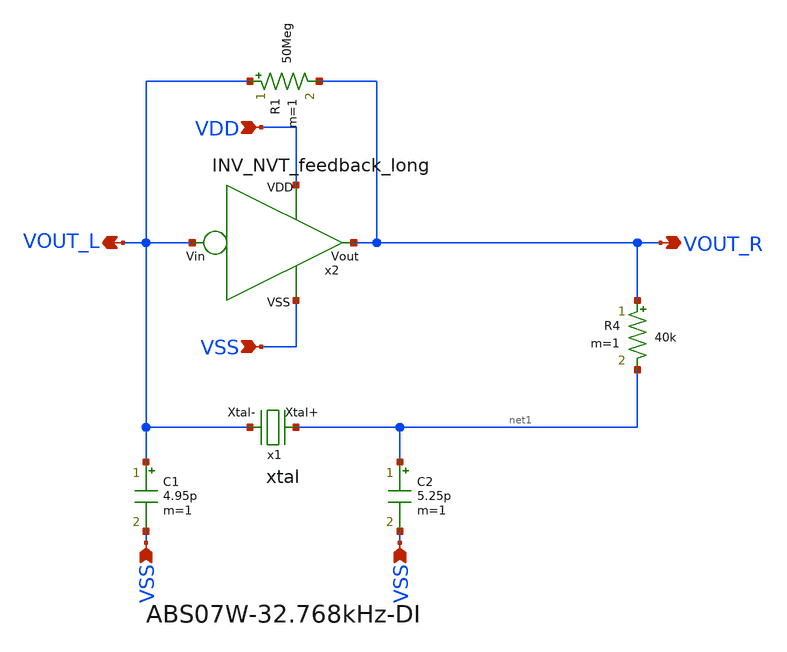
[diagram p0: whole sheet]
** sch_path: design/THESIS_EXP_RO_INVERTER_SKY130A/xtal_osc_NVT_L.sch
**.subckt xtal_osc_NVT_L VSS VSS VOUT_R VOUT_L VDD VSS
*.ipin VSS
*.ipin VSS
*.opin VOUT_R
*.opin VOUT_L
*.ipin VDD
*.ipin VSS
x1 net1 VOUT_L xtal
C1 VOUT_L VSS 4.95p m=1
C2 net1 VSS 5.25p m=1
R1 VOUT_L VOUT_R 50Meg m=1
R4 VOUT_R net1 40k m=1
x2 VDD VSS VOUT_R VOUT_L INV_NVT_feedback_long
**.ends

* expanding   symbol:  THESIS_EXP_RO_INVERTER_SKY130A/xtal.sym # of pins=2
** sym_path: design/THESIS_EXP_RO_INVERTER_SKY130A/xtal.sym
** sch_path: design/THESIS_EXP_RO_INVERTER_SKY130A/xtal.sch
.subckt xtal Xtal+ Xtal-
*.iopin Xtal+
*.iopin Xtal-
R1 Xtal+ net1 38.194k m=1
C1 net1 net2 4.68f m=1
L1 net2 Xtal- 5048.571 m=1
C2 Xtal+ Xtal- 1.15p m=1
.ends


* expanding   symbol:  THESIS_EXP_RO_INVERTER_SKY130A/INV_NVT_feedback_long.sym # of pins=4
** sym_path: design/THESIS_EXP_RO_INVERTER_SKY130A/INV_NVT_feedback_long.sym
** sch_path: design/THESIS_EXP_RO_INVERTER_SKY130A/INV_NVT_feedback_long.sch
.subckt INV_NVT_feedback_long VDD VSS Vout Vin
*.ipin VSS
*.ipin Vin
*.opin Vout
*.ipin VDD
XM1 Vout Vin VDD VDD sky130_fd_pr__pfet_01v8_lvt L=0.35 W=7 nf=1 ad='int((nf+1)/2) * W/nf * 0.29' as='int((nf+2)/2) * W/nf * 0.29'
+ pd='2*int((nf+1)/2) * (W/nf + 0.29)' ps='2*int((nf+2)/2) * (W/nf + 0.29)' nrd='0.29 / W' nrs='0.29 / W'
+ sa=0 sb=0 sd=0 mult=m_alpha m=m_alpha
XM2 Vout Vin vn VSS sky130_fd_pr__nfet_03v3_nvt L=0.8 W=0.42 nf=1 ad='int((nf+1)/2) * W/nf * 0.29' as='int((nf+2)/2) * W/nf * 0.29'
+ pd='2*int((nf+1)/2) * (W/nf + 0.29)' ps='2*int((nf+2)/2) * (W/nf + 0.29)' nrd='0.29 / W' nrs='0.29 / W'
+ sa=0 sb=0 sd=0 mult=m_beta m=m_beta
XM3 vn Vin VSS VSS sky130_fd_pr__nfet_03v3_nvt L=0.8 W=0.42 nf=1 ad='int((nf+1)/2) * W/nf * 0.29' as='int((nf+2)/2) * W/nf * 0.29'
+ pd='2*int((nf+1)/2) * (W/nf + 0.29)' ps='2*int((nf+2)/2) * (W/nf + 0.29)' nrd='0.29 / W' nrs='0.29 / W'
+ sa=0 sb=0 sd=0 mult=m_I0 m=m_I0
XM4 VDD Vout vn VSS sky130_fd_pr__nfet_03v3_nvt L=0.8 W=0.42 nf=1 ad='int((nf+1)/2) * W/nf * 0.29' as='int((nf+2)/2) * W/nf * 0.29'
+ pd='2*int((nf+1)/2) * (W/nf + 0.29)' ps='2*int((nf+2)/2) * (W/nf + 0.29)' nrd='0.29 / W' nrs='0.29 / W'
+ sa=0 sb=0 sd=0 mult=m_gamma m=m_gamma
.ends

.end
